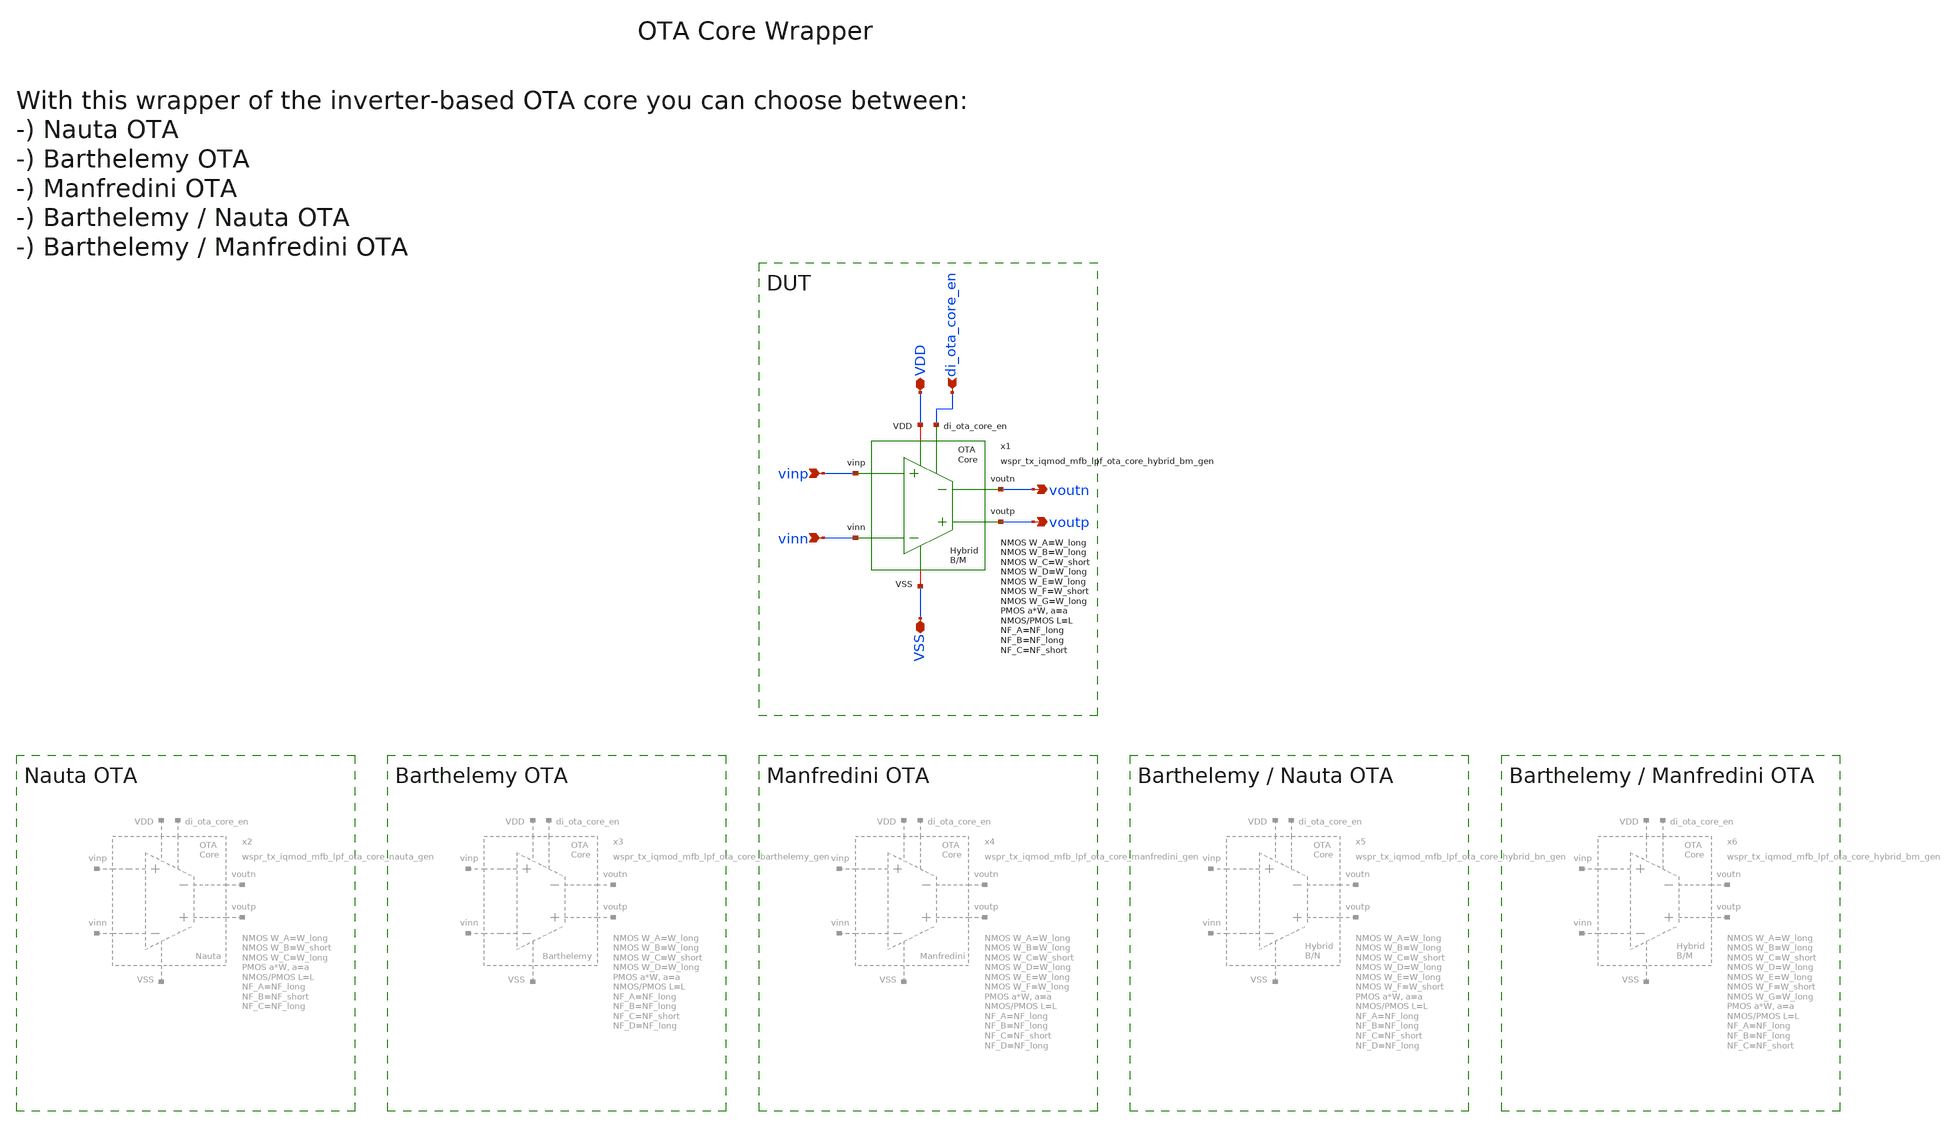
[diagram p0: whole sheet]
** sch_path: sky130/macros/iqmod/schematic/generic/wspr_tx_iqmod_mfb_lpf_ota_core_gen.sch
**.subckt wspr_tx_iqmod_mfb_lpf_ota_core_gen di_ota_core_en vinp vinn voutp voutn VDD VSS
*.ipin di_ota_core_en
*.ipin vinp
*.ipin vinn
*.opin voutp
*.opin voutn
*.iopin VDD
*.iopin VSS
x1 di_ota_core_en voutp voutn vinn vinp VDD VSS wspr_tx_iqmod_mfb_lpf_ota_core_hybrid_bm_gen
+ W_A=W_long W_B=W_long W_C=W_short W_D=W_long W_E=W_long W_F=W_short W_G=W_long a=a L=L NF_A=NF_long
+ NF_B=NF_long NF_C=NF_short NF_D=NF_long NF_E=NF_long NF_F=NF_short NF_G=NF_long
**.ends
.end
